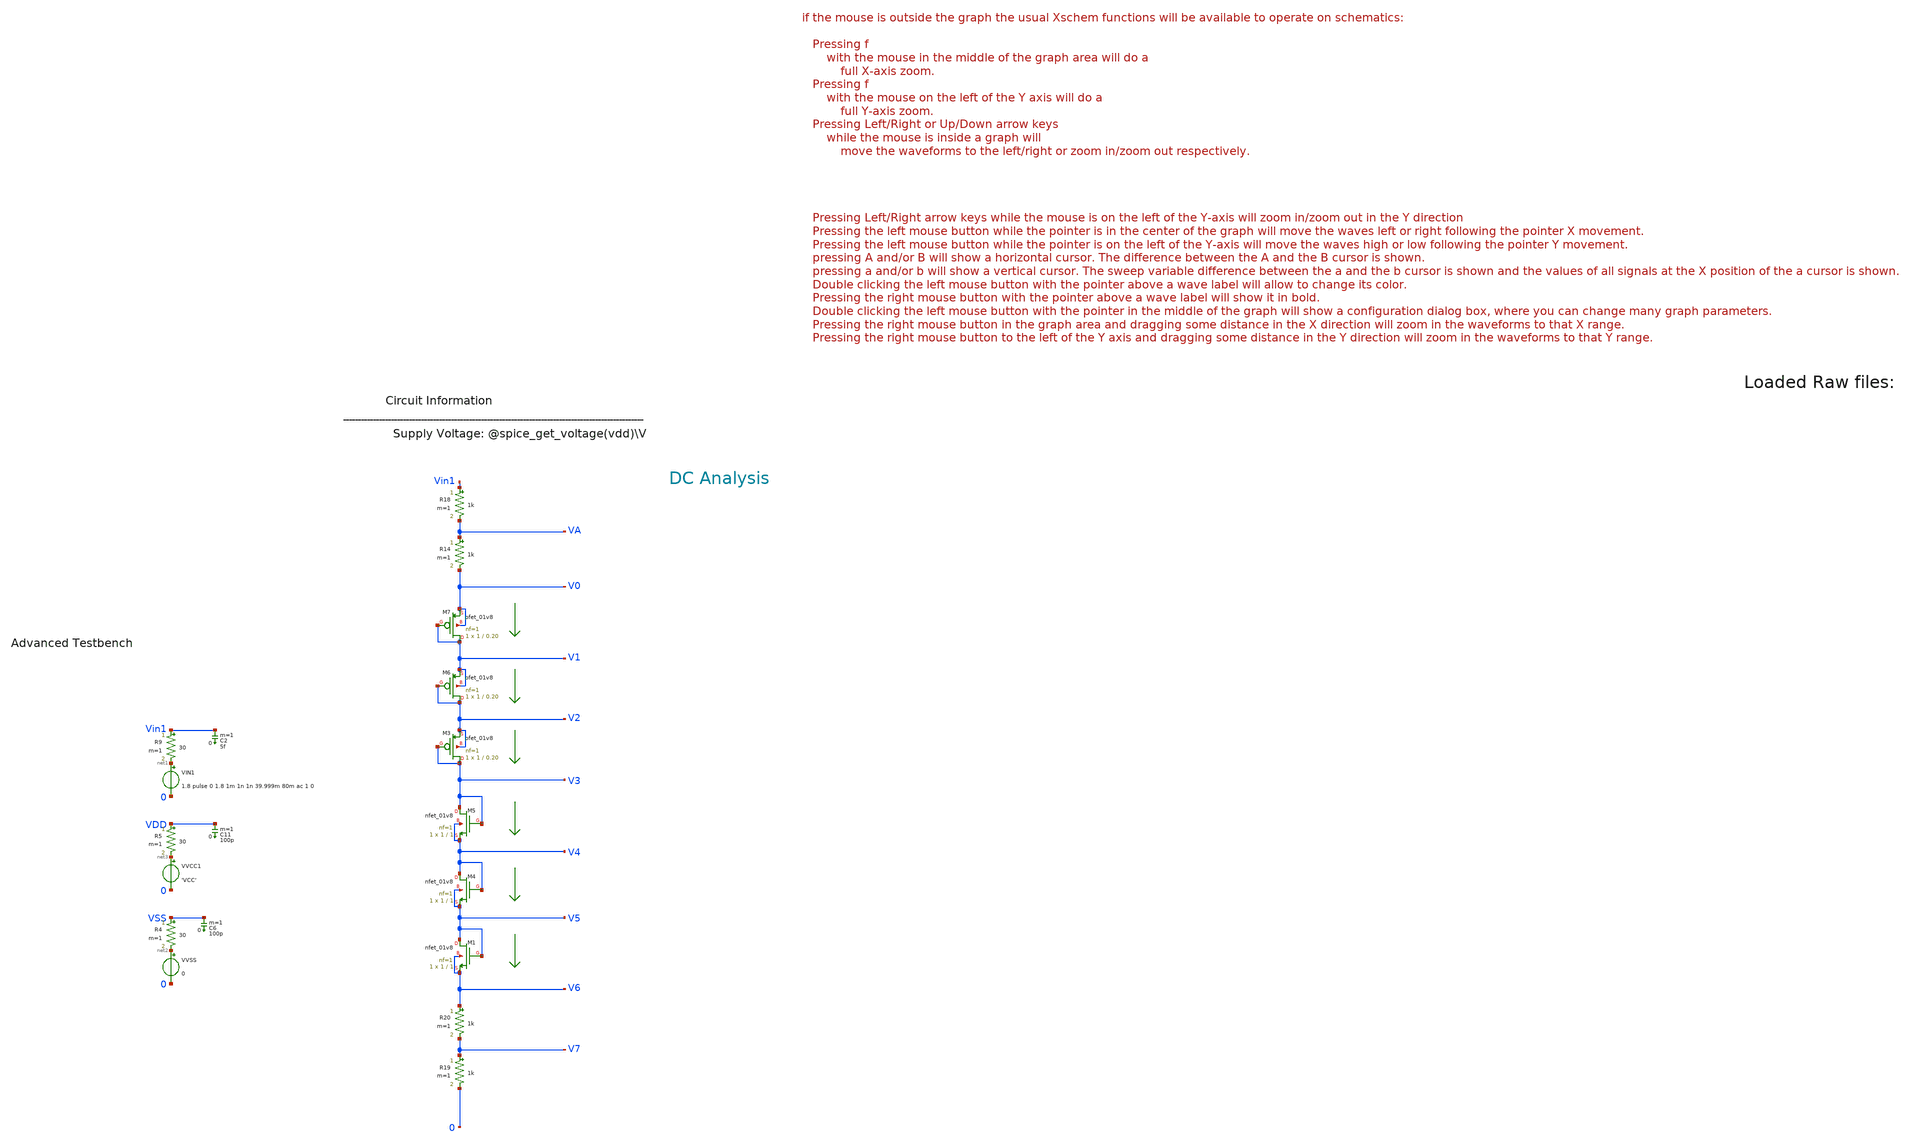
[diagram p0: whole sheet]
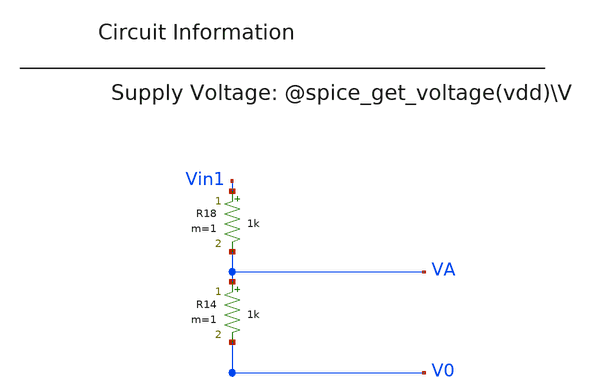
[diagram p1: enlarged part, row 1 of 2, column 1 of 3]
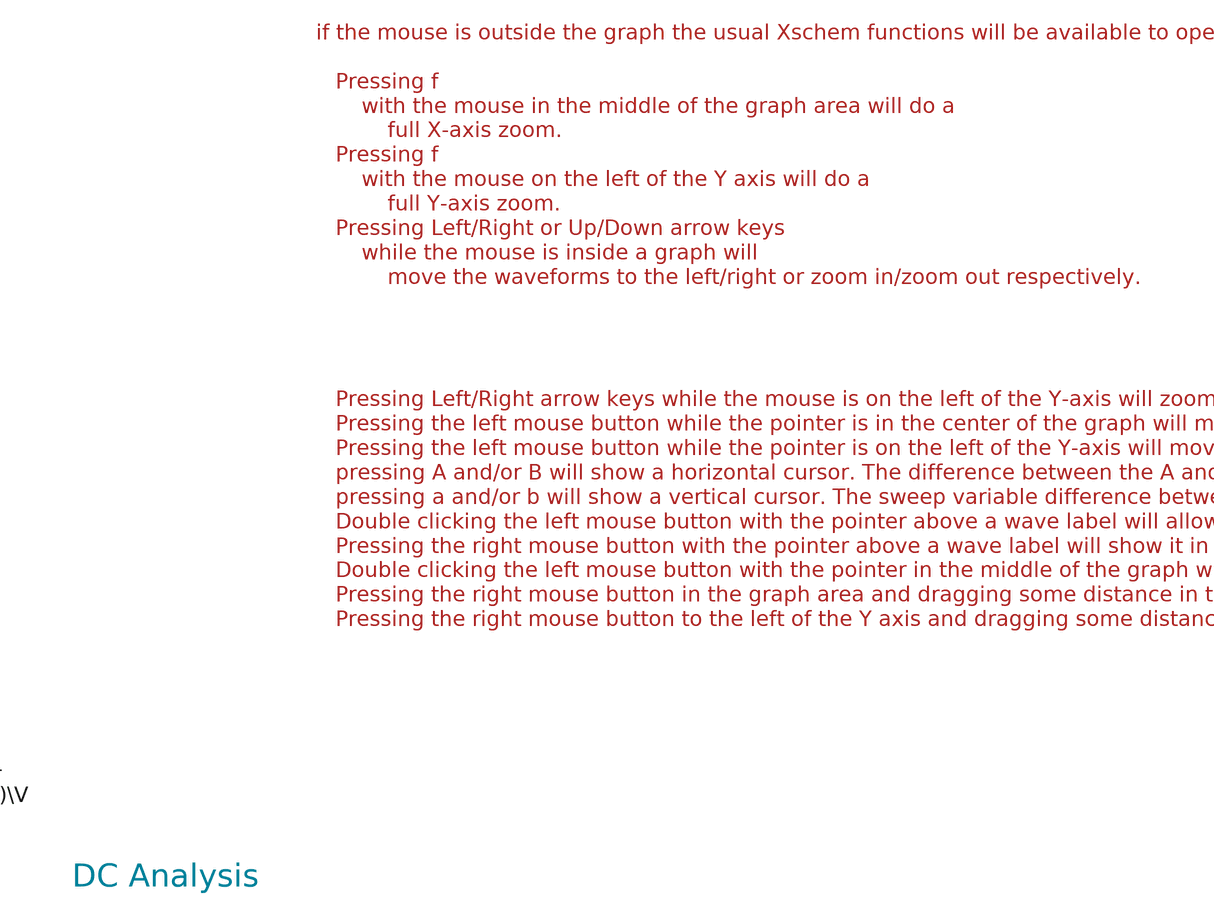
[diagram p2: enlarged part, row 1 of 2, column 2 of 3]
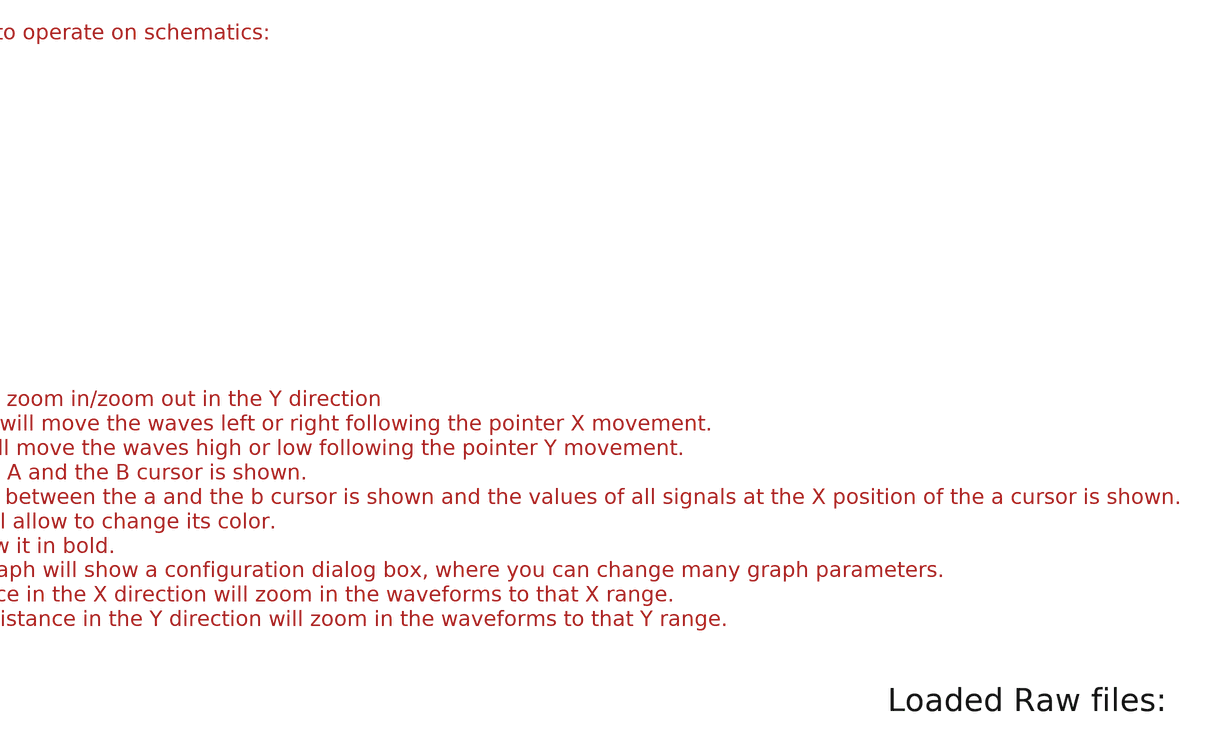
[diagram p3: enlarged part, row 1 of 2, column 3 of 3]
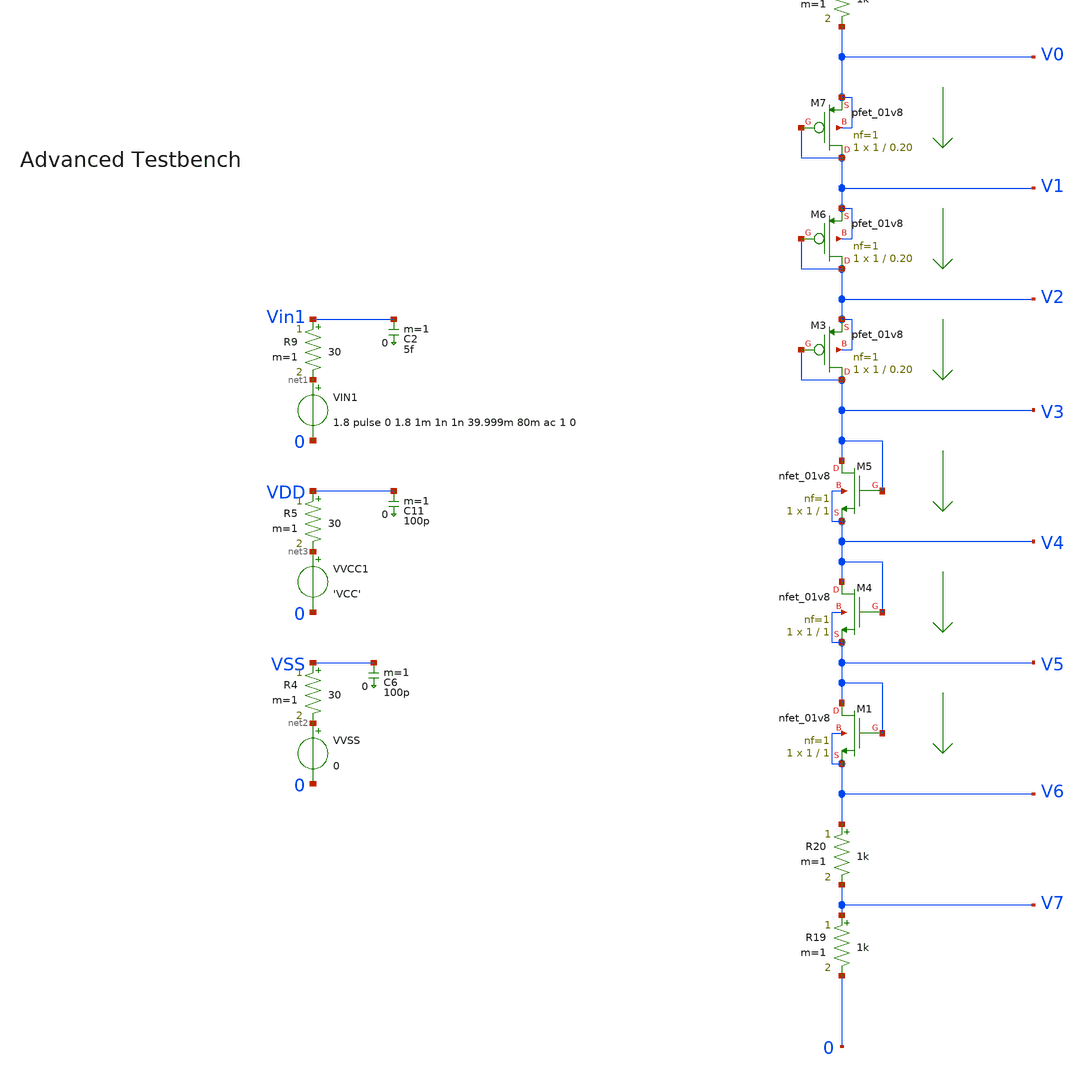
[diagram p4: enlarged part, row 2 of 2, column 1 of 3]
** sch_path: tt10-hdl/tt_um_test_commit/xschem/T0/mosDiode/mosDiode_tb.sch
* Copyright (C) 1998-2024 Stefan Frederik Schippers
* This program is free software; you can redistribute it and/or modify
* it under the terms of the GNU General Public License as published by
* the Free Software Foundation; either version 2 of the License, or
* (at your option) any later version.
* This program is distributed in the hope that it will be useful,
* but WITHOUT ANY WARRANTY; without even the implied warranty of
* MERCHANTABILITY or FITNESS FOR A PARTICULAR PURPOSE.  See the
* GNU General Public License for more details.
* You should have received a copy of the GNU General Public License
* along with this program; if not, write to the Free Software
**.subckt mosDiode_tb
VIN1 net1 0 1.8 pulse 0 1.8 1m 1n 1n 39.999m 80m ac 1 0
VVSS net2 0 0
R4 VSS net2 30 m=1
C6 VSS 0 100p m=1
VVCC1 net3 0 'VCC'
R5 VDD net3 30 m=1
C11 VDD 0 100p m=1
R9 Vin1 net1 30 m=1
C2 Vin1 0 5f m=1
XM1 V5 V5 V6 V6 sky130_fd_pr__nfet_01v8 L=1 W=1 nf=1 ad='int((1 + 1)/2) * 1 / 1 * 0.29' as='int((1 + 2)/2) * 1 / 1 * 0.29'
+ pd='2*int((1 + 1)/2) * (1 / 1 + 0.29)' ps='2*int((1 + 2)/2) * (1 / 1 + 0.29)' nrd='0.29 / 1 ' nrs='0.29 / 1 '
+ sa=0 sb=0 sd=0 mult=1 m=1
XM3 V3 V3 V2 V2 sky130_fd_pr__pfet_01v8 L=0.20 W=1 nf=1 ad='int((nf+1)/2) * W/nf * 0.29' as='int((nf+2)/2) * W/nf * 0.29'
+ pd='2*int((nf+1)/2) * (W/nf + 0.29)' ps='2*int((nf+2)/2) * (W/nf + 0.29)' nrd='0.29 / W' nrs='0.29 / W'
+ sa=0 sb=0 sd=0 mult=1 m=1
XM4 V4 V4 V5 V5 sky130_fd_pr__nfet_01v8 L=1 W=1 nf=1 ad='int((1 + 1)/2) * 1 / 1 * 0.29' as='int((1 + 2)/2) * 1 / 1 * 0.29'
+ pd='2*int((1 + 1)/2) * (1 / 1 + 0.29)' ps='2*int((1 + 2)/2) * (1 / 1 + 0.29)' nrd='0.29 / 1 ' nrs='0.29 / 1 '
+ sa=0 sb=0 sd=0 mult=1 m=1
XM5 V3 V3 V4 V4 sky130_fd_pr__nfet_01v8 L=1 W=1 nf=1 ad='int((1 + 1)/2) * 1 / 1 * 0.29' as='int((1 + 2)/2) * 1 / 1 * 0.29'
+ pd='2*int((1 + 1)/2) * (1 / 1 + 0.29)' ps='2*int((1 + 2)/2) * (1 / 1 + 0.29)' nrd='0.29 / 1 ' nrs='0.29 / 1 '
+ sa=0 sb=0 sd=0 mult=1 m=1
XM6 V2 V2 V1 V1 sky130_fd_pr__pfet_01v8 L=0.20 W=1 nf=1 ad='int((nf+1)/2) * W/nf * 0.29' as='int((nf+2)/2) * W/nf * 0.29'
+ pd='2*int((nf+1)/2) * (W/nf + 0.29)' ps='2*int((nf+2)/2) * (W/nf + 0.29)' nrd='0.29 / W' nrs='0.29 / W'
+ sa=0 sb=0 sd=0 mult=1 m=1
XM7 V1 V1 V0 V0 sky130_fd_pr__pfet_01v8 L=0.20 W=1 nf=1 ad='int((nf+1)/2) * W/nf * 0.29' as='int((nf+2)/2) * W/nf * 0.29'
+ pd='2*int((nf+1)/2) * (W/nf + 0.29)' ps='2*int((nf+2)/2) * (W/nf + 0.29)' nrd='0.29 / W' nrs='0.29 / W'
+ sa=0 sb=0 sd=0 mult=1 m=1
R14 VA V0 1k m=1
R18 Vin1 VA 1k m=1
R19 V7 0 1k m=1
R20 V6 V7 1k m=1
**** begin user architecture code



.temp 30
*.param IB=1n
.param VCC = 1.8

.option savecurrents
.save all @m1[gm]
.control
  save all alli
  op
  let power=-v(vcc) * i(vvcc)
  settype power power
  write template_adv_tb.raw
  set appendwrite

  dc vin1 0 1.8 0.005
  write template_adv_tb.raw

  tran 1u 2m
  *tran 0.01n 15n
  write template_adv_tb.raw

  *ac dec 10 1 1G
  *remzerovec
  *write template_adv_tb.raw



  quit 0




.endc





** opencircuitdesign pdks install
.lib $::SKYWATER_MODELS/sky130.lib.spice tt
.include $::SKYWATER_STDCELLS/sky130_fd_sc_hd.spice


**** end user architecture code
**.ends
.end
